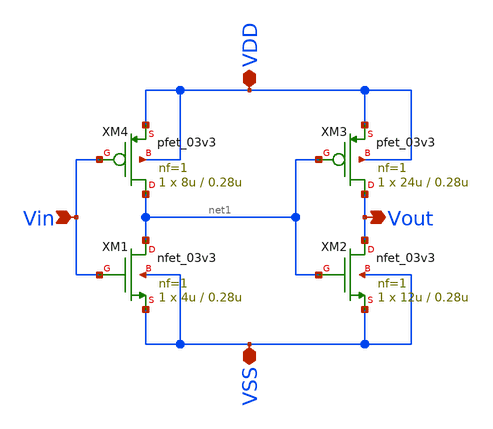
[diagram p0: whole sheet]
** sch_path: designs/simulation_parasitics/schematics/digital_input_buffer.sch
**.subckt digital_input_buffer VDD VSS Vin Vout
*.iopin VDD
*.iopin VSS
*.ipin Vin
*.opin Vout
XM1 net1 Vin VSS VSS nfet_03v3 L=0.28u W=4u nf=1 ad='int((nf+1)/2) * W/nf * 0.18u' as='int((nf+2)/2) * W/nf * 0.18u'
+ pd='2*int((nf+1)/2) * (W/nf + 0.18u)' ps='2*int((nf+2)/2) * (W/nf + 0.18u)' nrd='0.18u / W' nrs='0.18u / W'
+ sa=0 sb=0 sd=0 m=1
XM2 Vout net1 VSS VSS nfet_03v3 L=0.28u W=12u nf=1 ad='int((nf+1)/2) * W/nf * 0.18u' as='int((nf+2)/2) * W/nf * 0.18u'
+ pd='2*int((nf+1)/2) * (W/nf + 0.18u)' ps='2*int((nf+2)/2) * (W/nf + 0.18u)' nrd='0.18u / W' nrs='0.18u / W'
+ sa=0 sb=0 sd=0 m=1
XM3 Vout net1 VDD VDD pfet_03v3 L=0.28u W=24u nf=1 ad='int((nf+1)/2) * W/nf * 0.18u' as='int((nf+2)/2) * W/nf * 0.18u'
+ pd='2*int((nf+1)/2) * (W/nf + 0.18u)' ps='2*int((nf+2)/2) * (W/nf + 0.18u)' nrd='0.18u / W' nrs='0.18u / W'
+ sa=0 sb=0 sd=0 m=1
XM4 net1 Vin VDD VDD pfet_03v3 L=0.28u W=8u nf=1 ad='int((nf+1)/2) * W/nf * 0.18u' as='int((nf+2)/2) * W/nf * 0.18u'
+ pd='2*int((nf+1)/2) * (W/nf + 0.18u)' ps='2*int((nf+2)/2) * (W/nf + 0.18u)' nrd='0.18u / W' nrs='0.18u / W'
+ sa=0 sb=0 sd=0 m=1
**.ends
.end
